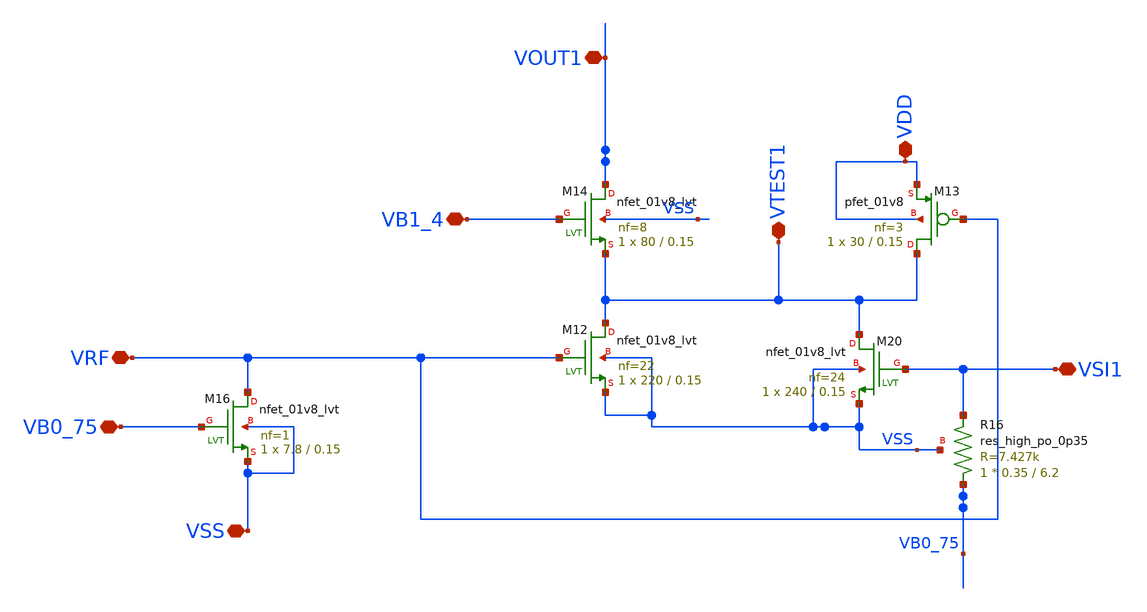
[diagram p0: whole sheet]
** sch_path: xschem/xschem4_sic_oct_20/partition1.sch
**.subckt partition1 VRF VSS VB0_75 VSI1 VB1_4 VTEST1 VOUT1 VDD
*.iopin VRF
*.iopin VSS
*.iopin VB0_75
*.iopin VSI1
*.iopin VB1_4
*.iopin VTEST1
*.iopin VOUT1
*.iopin VDD
XM12 VTEST1 VRF VSS VSS sky130_fd_pr__nfet_01v8_lvt L=0.15 W=220 nf=22 ad='int((nf+1)/2) * W/nf * 0.29'
+ as='int((nf+2)/2) * W/nf * 0.29' pd='2*int((nf+1)/2) * (W/nf + 0.29)' ps='2*int((nf+2)/2) * (W/nf + 0.29)'
+ nrd='0.29 / W' nrs='0.29 / W' sa=0 sb=0 sd=0 mult=1 m=1
XM13 VTEST1 VRF VDD VDD sky130_fd_pr__pfet_01v8 L=0.15 W=30 nf=3 ad='int((nf+1)/2) * W/nf * 0.29' as='int((nf+2)/2) * W/nf * 0.29'
+ pd='2*int((nf+1)/2) * (W/nf + 0.29)' ps='2*int((nf+2)/2) * (W/nf + 0.29)' nrd='0.29 / W' nrs='0.29 / W'
+ sa=0 sb=0 sd=0 mult=1 m=1
XM14 VOUT1 VB1_4 VTEST1 VSS sky130_fd_pr__nfet_01v8_lvt L=0.15 W=80 nf=8 ad='int((nf+1)/2) * W/nf * 0.29'
+ as='int((nf+2)/2) * W/nf * 0.29' pd='2*int((nf+1)/2) * (W/nf + 0.29)' ps='2*int((nf+2)/2) * (W/nf + 0.29)'
+ nrd='0.29 / W' nrs='0.29 / W' sa=0 sb=0 sd=0 mult=1 m=1
XM16 VRF VB0_75 VSS VSS sky130_fd_pr__nfet_01v8_lvt L=0.15 W=7.8 nf=1 ad='int((nf+1)/2) * W/nf * 0.29'
+ as='int((nf+2)/2) * W/nf * 0.29' pd='2*int((nf+1)/2) * (W/nf + 0.29)' ps='2*int((nf+2)/2) * (W/nf + 0.29)'
+ nrd='0.29 / W' nrs='0.29 / W' sa=0 sb=0 sd=0 mult=1 m=1
XM20 VTEST1 VSI1 VSS VSS sky130_fd_pr__nfet_01v8_lvt L=0.15 W=240 nf=24 ad='int((nf+1)/2) * W/nf * 0.29'
+ as='int((nf+2)/2) * W/nf * 0.29' pd='2*int((nf+1)/2) * (W/nf + 0.29)' ps='2*int((nf+2)/2) * (W/nf + 0.29)'
+ nrd='0.29 / W' nrs='0.29 / W' sa=0 sb=0 sd=0 mult=1 m=1
XR16 VB0_75 VSI1 VSS sky130_fd_pr__res_high_po_0p35 L=6.2 mult=1 m=1
**.ends
.end
